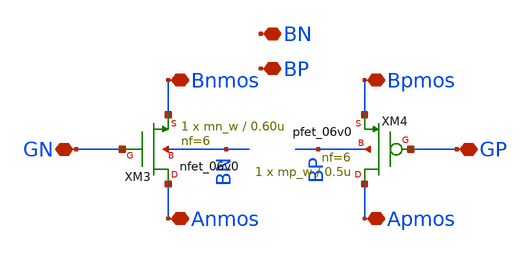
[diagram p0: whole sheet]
** sch_path: designs/switch_matrix_gf180mcu_9t5v0-main/tgate_PK_5V/transmission_gate_N_P_separate_5V.sch
**.subckt transmission_gate_N_P_separate_5V Bnmos GN Anmos GP BN BP Apmos Bpmos
*.iopin Bnmos
*.iopin GN
*.iopin Anmos
*.iopin GP
*.iopin BN
*.iopin BP
*.iopin Apmos
*.iopin Bpmos
XM3 Anmos GN Bnmos BN nfet_06v0 L=0.60u W=mn_w nf=6 ad='int((nf+1)/2) * W/nf * 0.18u' as='int((nf+2)/2) * W/nf * 0.18u'
+ pd='2*int((nf+1)/2) * (W/nf + 0.18u)' ps='2*int((nf+2)/2) * (W/nf + 0.18u)' nrd='0.18u / W' nrs='0.18u / W'
+ sa=0 sb=0 sd=0 m=1
XM4 Apmos GP Bpmos BP pfet_06v0 L=0.5u W=mp_w nf=6 ad='int((nf+1)/2) * W/nf * 0.18u' as='int((nf+2)/2) * W/nf * 0.18u'
+ pd='2*int((nf+1)/2) * (W/nf + 0.18u)' ps='2*int((nf+2)/2) * (W/nf + 0.18u)' nrd='0.18u / W' nrs='0.18u / W'
+ sa=0 sb=0 sd=0 m=1
**.ends
.end
